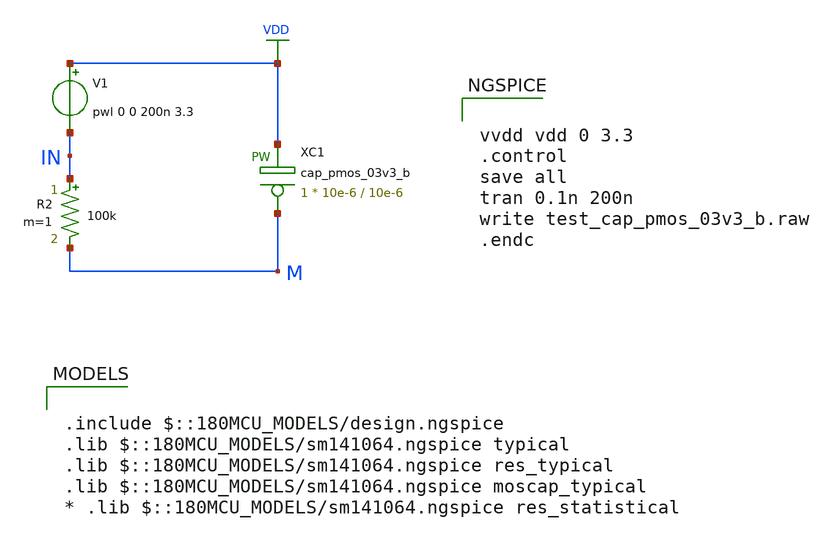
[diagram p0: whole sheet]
** sch_path: gf180mcuD/xschem_libs/gf180mcu_tests/test_cap_pmos_03v3_b/schematic/test_cap_pmos_03v3_b.sch
* Copyright 2022 GlobalFoundries PDK Authors
* Licensed under the Apache License, Version 2.0 (the "License");
* you may not use this file except in compliance with the License.
* You may obtain a copy of the License at
* https://www.apache.org/licenses/LICENSE-2.0
* Unless required by applicable law or agreed to in writing, software
* distributed under the License is distributed on an "AS IS" BASIS,
* WITHOUT WARRANTIES OR CONDITIONS OF ANY KIND, either express or implied.
* See the License for the specific language governing permissions and
* limitations under the License.
**.subckt test_cap_pmos_03v3_b
XC1 M VDD cap_pmos_03v3_b c_width=10e-6 c_length=10e-6 m=1
V1 VDD IN pwl 0 0 200n 3.3
R2 IN M 100k m=1
**** begin user architecture code

.include $::180MCU_MODELS/design.ngspice
.lib $::180MCU_MODELS/sm141064.ngspice typical
.lib $::180MCU_MODELS/sm141064.ngspice res_typical
.lib $::180MCU_MODELS/sm141064.ngspice moscap_typical
* .lib $::180MCU_MODELS/sm141064.ngspice res_statistical



vvdd vdd 0 3.3
.control
save all
tran 0.1n 200n
write test_cap_pmos_03v3_b.raw
.endc


**** end user architecture code
**.ends
.GLOBAL VDD
.end
